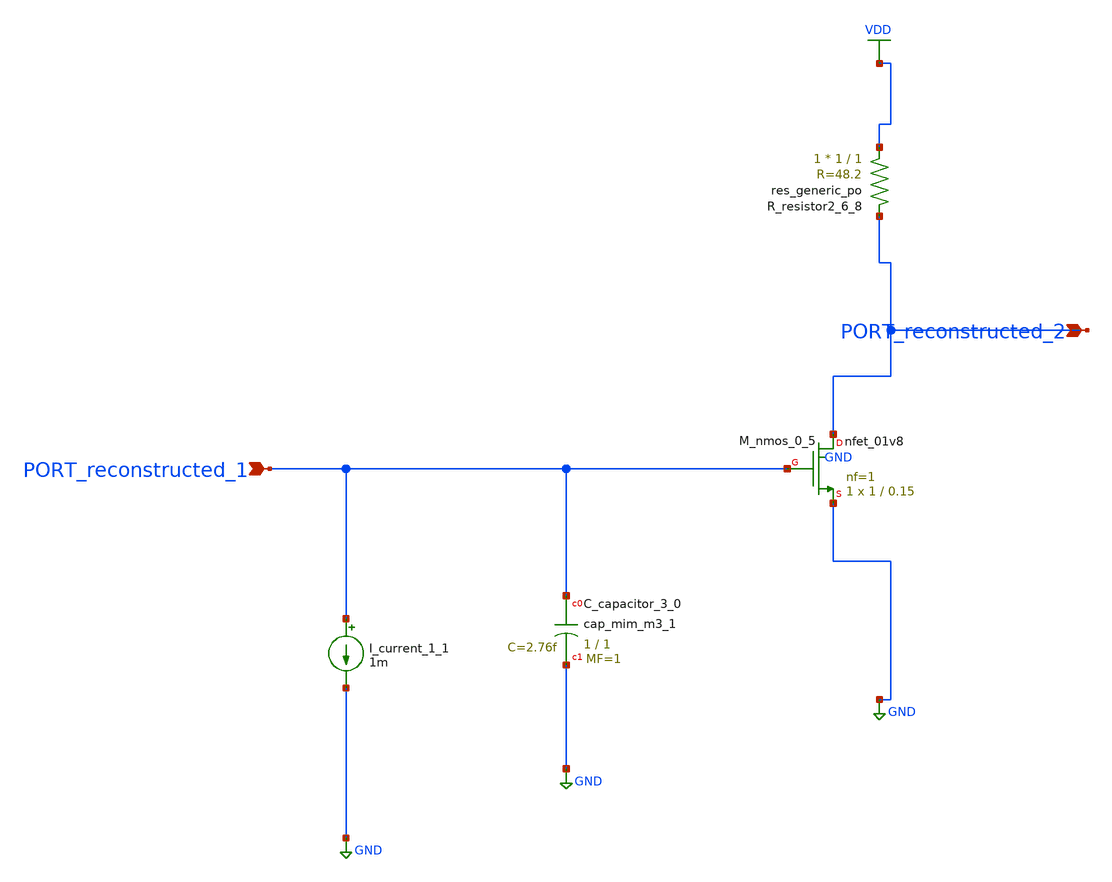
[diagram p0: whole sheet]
** sch_path: schematics/AMSNet/444.sch
**.subckt 444 PORT_reconstructed_2 PORT_reconstructed_1
*.ipin PORT_reconstructed_2
*.ipin PORT_reconstructed_1
XC_capacitor_3_0 PORT_reconstructed_1 GND sky130_fd_pr__cap_mim_m3_1 W=1 L=1 MF=1 m=1
I_current_1_1 PORT_reconstructed_1 GND 1m
XM_nmos_0_5 PORT_reconstructed_2 PORT_reconstructed_1 GND GND sky130_fd_pr__nfet_01v8 L=0.15 W=1 nf=1
+ ad='int((1 + 1)/2) * 1 / 1 * 0.29' as='int((1 + 2)/2) * 1 / 1 * 0.29' pd='2*int((1 + 1)/2) * (1 / 1 + 0.29)'
+ ps='2*int((1 + 2)/2) * (1 / 1 + 0.29)' nrd='0.29 / 1 ' nrs='0.29 / 1 ' sa=0 sb=0 sd=0 mult=1 m=1
XR_resistor2_6_8 VDD PORT_reconstructed_2 sky130_fd_pr__res_generic_po W=1 L=1 m=1
**.ends
.GLOBAL GND
.GLOBAL VDD
.end
